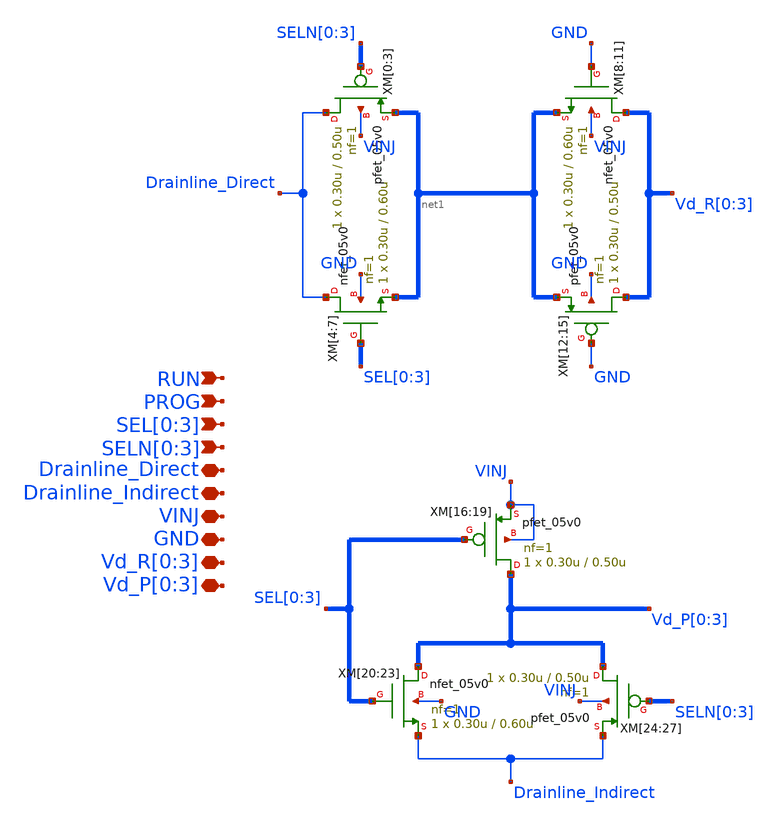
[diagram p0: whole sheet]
** sch_path: 4_Schematics/SWC_Drain.sch
**.subckt SWC_Drain RUN PROG SEL[0],SEL[1],SEL[2],SEL[3] SELN[0],SELN[1],SELN[2],SELN[3]
*+ Drainline_Direct Drainline_Indirect VINJ GND Vd_R[0],Vd_R[1],Vd_R[2],Vd_R[3] Vd_P[0],Vd_P[1],Vd_P[2],Vd_P[3]
*.ipin RUN
*.ipin PROG
*.ipin SEL[0],SEL[1],SEL[2],SEL[3]
*.ipin SELN[0],SELN[1],SELN[2],SELN[3]
*.iopin Drainline_Direct
*.iopin Drainline_Indirect
*.iopin VINJ
*.iopin GND
*.iopin Vd_R[0],Vd_R[1],Vd_R[2],Vd_R[3]
*.iopin Vd_P[0],Vd_P[1],Vd_P[2],Vd_P[3]
XM[4] Drainline_Direct SEL[0] net1[3] GND nfet_05v0 L=0.60u W=0.30u nf=1 ad='int((nf+1)/2) * W/nf * 0.18u'
+ as='int((nf+2)/2) * W/nf * 0.18u' pd='2*int((nf+1)/2) * (W/nf + 0.18u)' ps='2*int((nf+2)/2) * (W/nf + 0.18u)'
+ nrd='0.18u / W' nrs='0.18u / W' sa=0 sb=0 sd=0 m=1
XM[5] Drainline_Direct SEL[1] net1[2] GND nfet_05v0 L=0.60u W=0.30u nf=1 ad='int((nf+1)/2) * W/nf * 0.18u'
+ as='int((nf+2)/2) * W/nf * 0.18u' pd='2*int((nf+1)/2) * (W/nf + 0.18u)' ps='2*int((nf+2)/2) * (W/nf + 0.18u)'
+ nrd='0.18u / W' nrs='0.18u / W' sa=0 sb=0 sd=0 m=1
XM[6] Drainline_Direct SEL[2] net1[1] GND nfet_05v0 L=0.60u W=0.30u nf=1 ad='int((nf+1)/2) * W/nf * 0.18u'
+ as='int((nf+2)/2) * W/nf * 0.18u' pd='2*int((nf+1)/2) * (W/nf + 0.18u)' ps='2*int((nf+2)/2) * (W/nf + 0.18u)'
+ nrd='0.18u / W' nrs='0.18u / W' sa=0 sb=0 sd=0 m=1
XM[7] Drainline_Direct SEL[3] net1[0] GND nfet_05v0 L=0.60u W=0.30u nf=1 ad='int((nf+1)/2) * W/nf * 0.18u'
+ as='int((nf+2)/2) * W/nf * 0.18u' pd='2*int((nf+1)/2) * (W/nf + 0.18u)' ps='2*int((nf+2)/2) * (W/nf + 0.18u)'
+ nrd='0.18u / W' nrs='0.18u / W' sa=0 sb=0 sd=0 m=1
XM[0] Drainline_Direct SELN[0] net1[3] VINJ pfet_05v0 L=0.50u W=0.30u nf=1 ad='int((nf+1)/2) * W/nf * 0.18u'
+ as='int((nf+2)/2) * W/nf * 0.18u' pd='2*int((nf+1)/2) * (W/nf + 0.18u)' ps='2*int((nf+2)/2) * (W/nf + 0.18u)'
+ nrd='0.18u / W' nrs='0.18u / W' sa=0 sb=0 sd=0 m=1
XM[1] Drainline_Direct SELN[1] net1[2] VINJ pfet_05v0 L=0.50u W=0.30u nf=1 ad='int((nf+1)/2) * W/nf * 0.18u'
+ as='int((nf+2)/2) * W/nf * 0.18u' pd='2*int((nf+1)/2) * (W/nf + 0.18u)' ps='2*int((nf+2)/2) * (W/nf + 0.18u)'
+ nrd='0.18u / W' nrs='0.18u / W' sa=0 sb=0 sd=0 m=1
XM[2] Drainline_Direct SELN[2] net1[1] VINJ pfet_05v0 L=0.50u W=0.30u nf=1 ad='int((nf+1)/2) * W/nf * 0.18u'
+ as='int((nf+2)/2) * W/nf * 0.18u' pd='2*int((nf+1)/2) * (W/nf + 0.18u)' ps='2*int((nf+2)/2) * (W/nf + 0.18u)'
+ nrd='0.18u / W' nrs='0.18u / W' sa=0 sb=0 sd=0 m=1
XM[3] Drainline_Direct SELN[3] net1[0] VINJ pfet_05v0 L=0.50u W=0.30u nf=1 ad='int((nf+1)/2) * W/nf * 0.18u'
+ as='int((nf+2)/2) * W/nf * 0.18u' pd='2*int((nf+1)/2) * (W/nf + 0.18u)' ps='2*int((nf+2)/2) * (W/nf + 0.18u)'
+ nrd='0.18u / W' nrs='0.18u / W' sa=0 sb=0 sd=0 m=1
XM[8] Vd_R[0] GND net1[3] VINJ nfet_05v0 L=0.60u W=0.30u nf=1 ad='int((nf+1)/2) * W/nf * 0.18u' as='int((nf+2)/2) * W/nf * 0.18u'
+ pd='2*int((nf+1)/2) * (W/nf + 0.18u)' ps='2*int((nf+2)/2) * (W/nf + 0.18u)' nrd='0.18u / W' nrs='0.18u / W'
+ sa=0 sb=0 sd=0 m=1
XM[9] Vd_R[1] GND net1[2] VINJ nfet_05v0 L=0.60u W=0.30u nf=1 ad='int((nf+1)/2) * W/nf * 0.18u' as='int((nf+2)/2) * W/nf * 0.18u'
+ pd='2*int((nf+1)/2) * (W/nf + 0.18u)' ps='2*int((nf+2)/2) * (W/nf + 0.18u)' nrd='0.18u / W' nrs='0.18u / W'
+ sa=0 sb=0 sd=0 m=1
XM[10] Vd_R[2] GND net1[1] VINJ nfet_05v0 L=0.60u W=0.30u nf=1 ad='int((nf+1)/2) * W/nf * 0.18u' as='int((nf+2)/2) * W/nf * 0.18u'
+ pd='2*int((nf+1)/2) * (W/nf + 0.18u)' ps='2*int((nf+2)/2) * (W/nf + 0.18u)' nrd='0.18u / W' nrs='0.18u / W'
+ sa=0 sb=0 sd=0 m=1
XM[11] Vd_R[3] GND net1[0] VINJ nfet_05v0 L=0.60u W=0.30u nf=1 ad='int((nf+1)/2) * W/nf * 0.18u' as='int((nf+2)/2) * W/nf * 0.18u'
+ pd='2*int((nf+1)/2) * (W/nf + 0.18u)' ps='2*int((nf+2)/2) * (W/nf + 0.18u)' nrd='0.18u / W' nrs='0.18u / W'
+ sa=0 sb=0 sd=0 m=1
XM[12] Vd_R[0] GND net1[3] GND pfet_05v0 L=0.50u W=0.30u nf=1 ad='int((nf+1)/2) * W/nf * 0.18u' as='int((nf+2)/2) * W/nf * 0.18u'
+ pd='2*int((nf+1)/2) * (W/nf + 0.18u)' ps='2*int((nf+2)/2) * (W/nf + 0.18u)' nrd='0.18u / W' nrs='0.18u / W'
+ sa=0 sb=0 sd=0 m=1
XM[13] Vd_R[1] GND net1[2] GND pfet_05v0 L=0.50u W=0.30u nf=1 ad='int((nf+1)/2) * W/nf * 0.18u' as='int((nf+2)/2) * W/nf * 0.18u'
+ pd='2*int((nf+1)/2) * (W/nf + 0.18u)' ps='2*int((nf+2)/2) * (W/nf + 0.18u)' nrd='0.18u / W' nrs='0.18u / W'
+ sa=0 sb=0 sd=0 m=1
XM[14] Vd_R[2] GND net1[1] GND pfet_05v0 L=0.50u W=0.30u nf=1 ad='int((nf+1)/2) * W/nf * 0.18u' as='int((nf+2)/2) * W/nf * 0.18u'
+ pd='2*int((nf+1)/2) * (W/nf + 0.18u)' ps='2*int((nf+2)/2) * (W/nf + 0.18u)' nrd='0.18u / W' nrs='0.18u / W'
+ sa=0 sb=0 sd=0 m=1
XM[15] Vd_R[3] GND net1[0] GND pfet_05v0 L=0.50u W=0.30u nf=1 ad='int((nf+1)/2) * W/nf * 0.18u' as='int((nf+2)/2) * W/nf * 0.18u'
+ pd='2*int((nf+1)/2) * (W/nf + 0.18u)' ps='2*int((nf+2)/2) * (W/nf + 0.18u)' nrd='0.18u / W' nrs='0.18u / W'
+ sa=0 sb=0 sd=0 m=1
XM[20] Vd_P[0] SEL[0] Drainline_Indirect GND nfet_05v0 L=0.60u W=0.30u nf=1 ad='int((nf+1)/2) * W/nf * 0.18u'
+ as='int((nf+2)/2) * W/nf * 0.18u' pd='2*int((nf+1)/2) * (W/nf + 0.18u)' ps='2*int((nf+2)/2) * (W/nf + 0.18u)'
+ nrd='0.18u / W' nrs='0.18u / W' sa=0 sb=0 sd=0 m=1
XM[21] Vd_P[1] SEL[1] Drainline_Indirect GND nfet_05v0 L=0.60u W=0.30u nf=1 ad='int((nf+1)/2) * W/nf * 0.18u'
+ as='int((nf+2)/2) * W/nf * 0.18u' pd='2*int((nf+1)/2) * (W/nf + 0.18u)' ps='2*int((nf+2)/2) * (W/nf + 0.18u)'
+ nrd='0.18u / W' nrs='0.18u / W' sa=0 sb=0 sd=0 m=1
XM[22] Vd_P[2] SEL[2] Drainline_Indirect GND nfet_05v0 L=0.60u W=0.30u nf=1 ad='int((nf+1)/2) * W/nf * 0.18u'
+ as='int((nf+2)/2) * W/nf * 0.18u' pd='2*int((nf+1)/2) * (W/nf + 0.18u)' ps='2*int((nf+2)/2) * (W/nf + 0.18u)'
+ nrd='0.18u / W' nrs='0.18u / W' sa=0 sb=0 sd=0 m=1
XM[23] Vd_P[3] SEL[3] Drainline_Indirect GND nfet_05v0 L=0.60u W=0.30u nf=1 ad='int((nf+1)/2) * W/nf * 0.18u'
+ as='int((nf+2)/2) * W/nf * 0.18u' pd='2*int((nf+1)/2) * (W/nf + 0.18u)' ps='2*int((nf+2)/2) * (W/nf + 0.18u)'
+ nrd='0.18u / W' nrs='0.18u / W' sa=0 sb=0 sd=0 m=1
XM[24] Vd_P[0] SELN[0] Drainline_Indirect VINJ pfet_05v0 L=0.50u W=0.30u nf=1 ad='int((nf+1)/2) * W/nf * 0.18u'
+ as='int((nf+2)/2) * W/nf * 0.18u' pd='2*int((nf+1)/2) * (W/nf + 0.18u)' ps='2*int((nf+2)/2) * (W/nf + 0.18u)'
+ nrd='0.18u / W' nrs='0.18u / W' sa=0 sb=0 sd=0 m=1
XM[25] Vd_P[1] SELN[1] Drainline_Indirect VINJ pfet_05v0 L=0.50u W=0.30u nf=1 ad='int((nf+1)/2) * W/nf * 0.18u'
+ as='int((nf+2)/2) * W/nf * 0.18u' pd='2*int((nf+1)/2) * (W/nf + 0.18u)' ps='2*int((nf+2)/2) * (W/nf + 0.18u)'
+ nrd='0.18u / W' nrs='0.18u / W' sa=0 sb=0 sd=0 m=1
XM[26] Vd_P[2] SELN[2] Drainline_Indirect VINJ pfet_05v0 L=0.50u W=0.30u nf=1 ad='int((nf+1)/2) * W/nf * 0.18u'
+ as='int((nf+2)/2) * W/nf * 0.18u' pd='2*int((nf+1)/2) * (W/nf + 0.18u)' ps='2*int((nf+2)/2) * (W/nf + 0.18u)'
+ nrd='0.18u / W' nrs='0.18u / W' sa=0 sb=0 sd=0 m=1
XM[27] Vd_P[3] SELN[3] Drainline_Indirect VINJ pfet_05v0 L=0.50u W=0.30u nf=1 ad='int((nf+1)/2) * W/nf * 0.18u'
+ as='int((nf+2)/2) * W/nf * 0.18u' pd='2*int((nf+1)/2) * (W/nf + 0.18u)' ps='2*int((nf+2)/2) * (W/nf + 0.18u)'
+ nrd='0.18u / W' nrs='0.18u / W' sa=0 sb=0 sd=0 m=1
XM[16] Vd_P[0] SEL[0] VINJ VINJ pfet_05v0 L=0.50u W=0.30u nf=1 ad='int((nf+1)/2) * W/nf * 0.18u' as='int((nf+2)/2) * W/nf * 0.18u'
+ pd='2*int((nf+1)/2) * (W/nf + 0.18u)' ps='2*int((nf+2)/2) * (W/nf + 0.18u)' nrd='0.18u / W' nrs='0.18u / W'
+ sa=0 sb=0 sd=0 m=1
XM[17] Vd_P[1] SEL[1] VINJ VINJ pfet_05v0 L=0.50u W=0.30u nf=1 ad='int((nf+1)/2) * W/nf * 0.18u' as='int((nf+2)/2) * W/nf * 0.18u'
+ pd='2*int((nf+1)/2) * (W/nf + 0.18u)' ps='2*int((nf+2)/2) * (W/nf + 0.18u)' nrd='0.18u / W' nrs='0.18u / W'
+ sa=0 sb=0 sd=0 m=1
XM[18] Vd_P[2] SEL[2] VINJ VINJ pfet_05v0 L=0.50u W=0.30u nf=1 ad='int((nf+1)/2) * W/nf * 0.18u' as='int((nf+2)/2) * W/nf * 0.18u'
+ pd='2*int((nf+1)/2) * (W/nf + 0.18u)' ps='2*int((nf+2)/2) * (W/nf + 0.18u)' nrd='0.18u / W' nrs='0.18u / W'
+ sa=0 sb=0 sd=0 m=1
XM[19] Vd_P[3] SEL[3] VINJ VINJ pfet_05v0 L=0.50u W=0.30u nf=1 ad='int((nf+1)/2) * W/nf * 0.18u' as='int((nf+2)/2) * W/nf * 0.18u'
+ pd='2*int((nf+1)/2) * (W/nf + 0.18u)' ps='2*int((nf+2)/2) * (W/nf + 0.18u)' nrd='0.18u / W' nrs='0.18u / W'
+ sa=0 sb=0 sd=0 m=1
**.ends
.end
